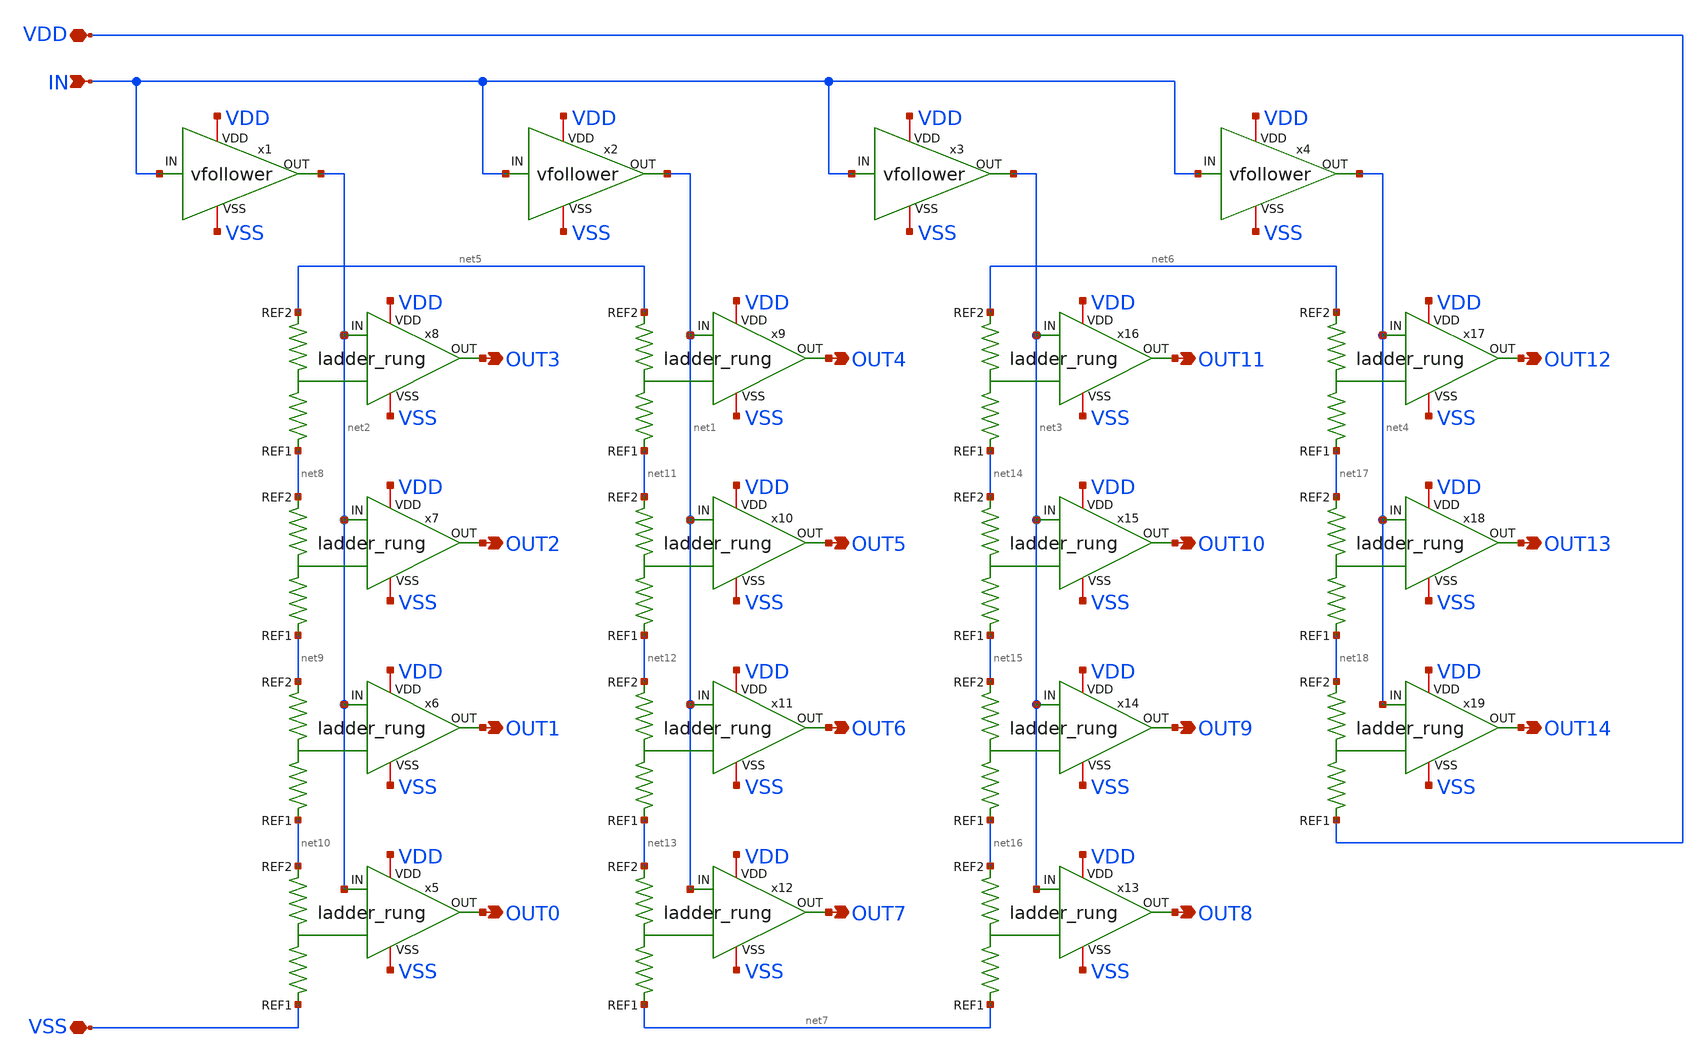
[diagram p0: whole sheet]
** sch_path: xschem/flash_adc.sch
**.subckt flash_adc VDD VSS IN OUT0 OUT1 OUT2 OUT3 OUT4 OUT5 OUT6 OUT7 OUT8 OUT9 OUT10 OUT11 OUT12
*+ OUT13 OUT14
*.iopin VDD
*.iopin VSS
*.ipin IN
*.opin OUT0
*.opin OUT1
*.opin OUT2
*.opin OUT3
*.opin OUT4
*.opin OUT5
*.opin OUT6
*.opin OUT7
*.opin OUT8
*.opin OUT9
*.opin OUT10
*.opin OUT11
*.opin OUT12
*.opin OUT13
*.opin OUT14
x1 VDD net2 IN VSS vfollower
x2 VDD net1 IN VSS vfollower
x3 VDD net3 IN VSS vfollower
x4 VDD net4 IN VSS vfollower
x5 net10 VDD net2 OUT0 VSS VSS ladder_rung
x6 net9 VDD net2 OUT1 VSS net10 ladder_rung
x7 net8 VDD net2 OUT2 VSS net9 ladder_rung
x8 net5 VDD net2 OUT3 VSS net8 ladder_rung
x9 net5 VDD net1 OUT4 VSS net11 ladder_rung
x10 net11 VDD net1 OUT5 VSS net12 ladder_rung
x11 net12 VDD net1 OUT6 VSS net13 ladder_rung
x12 net13 VDD net1 OUT7 VSS net7 ladder_rung
x13 net16 VDD net3 OUT8 VSS net7 ladder_rung
x14 net15 VDD net3 OUT9 VSS net16 ladder_rung
x15 net14 VDD net3 OUT10 VSS net15 ladder_rung
x16 net6 VDD net3 OUT11 VSS net14 ladder_rung
x17 net6 VDD net4 OUT12 VSS net17 ladder_rung
x18 net17 VDD net4 OUT13 VSS net18 ladder_rung
x19 net18 VDD net4 OUT14 VSS VDD ladder_rung
**.ends

* expanding   symbol:  vfollower.sym # of pins=4
** sym_path: xschem/vfollower.sym
** sch_path: xschem/vfollower.sch
.subckt vfollower VDD OUT IN VSS
*.iopin VDD
*.iopin VSS
*.ipin IN
*.opin OUT
x1 VDD OUT IN OUT VSS opamp
.ends


* expanding   symbol:  ladder_rung.sym # of pins=6
** sym_path: xschem/ladder_rung.sym
** sch_path: xschem/ladder_rung.sch
.subckt ladder_rung REF2 VDD IN OUT VSS REF1
*.opin OUT
*.iopin VDD
*.iopin VSS
*.ipin IN
*.iopin REF1
*.iopin REF2
XR1 REF1 net1 VSS sky130_fd_pr__res_xhigh_po_0p35 L=2.34 mult=1 m=1
x5 VDD OUT IN net1 VSS comparator
XR2 net1 REF2 VSS sky130_fd_pr__res_xhigh_po_0p35 L=2.34 mult=1 m=1
.ends


* expanding   symbol:  opamp.sym # of pins=5
** sym_path: xschem/opamp.sym
** sch_path: xschem/opamp.sch
.subckt opamp VDD OUT P N VSS
*.iopin VDD
*.iopin VSS
*.ipin P
*.ipin N
*.opin OUT
XR1 net2 VDD VSS sky130_fd_pr__res_xhigh_po_0p35 L=24.36 mult=1 m=1
XM1 net2 net2 VSS VSS sky130_fd_pr__nfet_g5v0d10v5 L=1 W=2 nf=1 ad='int((nf+1)/2) * W/nf * 0.29' as='int((nf+2)/2) * W/nf * 0.29'
+ pd='2*int((nf+1)/2) * (W/nf + 0.29)' ps='2*int((nf+2)/2) * (W/nf + 0.29)' nrd='0.29 / W' nrs='0.29 / W'
+ sa=0 sb=0 sd=0 mult=2 m=2
XM7 net1 net1 VDD VDD sky130_fd_pr__pfet_g5v0d10v5 L=1 W=4 nf=1 ad='int((nf+1)/2) * W/nf * 0.29' as='int((nf+2)/2) * W/nf * 0.29'
+ pd='2*int((nf+1)/2) * (W/nf + 0.29)' ps='2*int((nf+2)/2) * (W/nf + 0.29)' nrd='0.29 / W' nrs='0.29 / W'
+ sa=0 sb=0 sd=0 mult=2 m=2
XM8 OUT net1 VDD VDD sky130_fd_pr__pfet_g5v0d10v5 L=1 W=4 nf=1 ad='int((nf+1)/2) * W/nf * 0.29' as='int((nf+2)/2) * W/nf * 0.29'
+ pd='2*int((nf+1)/2) * (W/nf + 0.29)' ps='2*int((nf+2)/2) * (W/nf + 0.29)' nrd='0.29 / W' nrs='0.29 / W'
+ sa=0 sb=0 sd=0 mult=2 m=2
XM4 net6 net2 VSS VSS sky130_fd_pr__nfet_g5v0d10v5 L=1 W=2 nf=1 ad='int((nf+1)/2) * W/nf * 0.29' as='int((nf+2)/2) * W/nf * 0.29'
+ pd='2*int((nf+1)/2) * (W/nf + 0.29)' ps='2*int((nf+2)/2) * (W/nf + 0.29)' nrd='0.29 / W' nrs='0.29 / W'
+ sa=0 sb=0 sd=0 mult=2 m=2
XM5 net1 P net6 VSS sky130_fd_pr__nfet_g5v0d10v5 L=1 W=2 nf=1 ad='int((nf+1)/2) * W/nf * 0.29' as='int((nf+2)/2) * W/nf * 0.29'
+ pd='2*int((nf+1)/2) * (W/nf + 0.29)' ps='2*int((nf+2)/2) * (W/nf + 0.29)' nrd='0.29 / W' nrs='0.29 / W'
+ sa=0 sb=0 sd=0 mult=2 m=2
XM6 OUT N net6 VSS sky130_fd_pr__nfet_g5v0d10v5 L=1 W=2 nf=1 ad='int((nf+1)/2) * W/nf * 0.29' as='int((nf+2)/2) * W/nf * 0.29'
+ pd='2*int((nf+1)/2) * (W/nf + 0.29)' ps='2*int((nf+2)/2) * (W/nf + 0.29)' nrd='0.29 / W' nrs='0.29 / W'
+ sa=0 sb=0 sd=0 mult=2 m=2
XM2 net5 net2 VSS VSS sky130_fd_pr__nfet_g5v0d10v5 L=1 W=2 nf=1 ad='int((nf+1)/2) * W/nf * 0.29' as='int((nf+2)/2) * W/nf * 0.29'
+ pd='2*int((nf+1)/2) * (W/nf + 0.29)' ps='2*int((nf+2)/2) * (W/nf + 0.29)' nrd='0.29 / W' nrs='0.29 / W'
+ sa=0 sb=0 sd=0 mult=2 m=2
XM9 net4 net5 VDD VDD sky130_fd_pr__pfet_g5v0d10v5 L=1 W=4 nf=1 ad='int((nf+1)/2) * W/nf * 0.29' as='int((nf+2)/2) * W/nf * 0.29'
+ pd='2*int((nf+1)/2) * (W/nf + 0.29)' ps='2*int((nf+2)/2) * (W/nf + 0.29)' nrd='0.29 / W' nrs='0.29 / W'
+ sa=0 sb=0 sd=0 mult=2 m=2
XM3 VDD net5 net5 VDD sky130_fd_pr__pfet_g5v0d10v5 L=1 W=4 nf=1 ad='int((nf+1)/2) * W/nf * 0.29' as='int((nf+2)/2) * W/nf * 0.29'
+ pd='2*int((nf+1)/2) * (W/nf + 0.29)' ps='2*int((nf+2)/2) * (W/nf + 0.29)' nrd='0.29 / W' nrs='0.29 / W'
+ sa=0 sb=0 sd=0 mult=2 m=2
XM10 net3 P net4 VDD sky130_fd_pr__pfet_g5v0d10v5 L=1 W=4 nf=1 ad='int((nf+1)/2) * W/nf * 0.29' as='int((nf+2)/2) * W/nf * 0.29'
+ pd='2*int((nf+1)/2) * (W/nf + 0.29)' ps='2*int((nf+2)/2) * (W/nf + 0.29)' nrd='0.29 / W' nrs='0.29 / W'
+ sa=0 sb=0 sd=0 mult=2 m=2
XM11 OUT N net4 VDD sky130_fd_pr__pfet_g5v0d10v5 L=1 W=4 nf=1 ad='int((nf+1)/2) * W/nf * 0.29' as='int((nf+2)/2) * W/nf * 0.29'
+ pd='2*int((nf+1)/2) * (W/nf + 0.29)' ps='2*int((nf+2)/2) * (W/nf + 0.29)' nrd='0.29 / W' nrs='0.29 / W'
+ sa=0 sb=0 sd=0 mult=2 m=2
XM12 net3 net3 VSS VSS sky130_fd_pr__nfet_g5v0d10v5 L=1 W=2 nf=1 ad='int((nf+1)/2) * W/nf * 0.29' as='int((nf+2)/2) * W/nf * 0.29'
+ pd='2*int((nf+1)/2) * (W/nf + 0.29)' ps='2*int((nf+2)/2) * (W/nf + 0.29)' nrd='0.29 / W' nrs='0.29 / W'
+ sa=0 sb=0 sd=0 mult=2 m=2
XM13 OUT net3 VSS VSS sky130_fd_pr__nfet_g5v0d10v5 L=1 W=2 nf=1 ad='int((nf+1)/2) * W/nf * 0.29' as='int((nf+2)/2) * W/nf * 0.29'
+ pd='2*int((nf+1)/2) * (W/nf + 0.29)' ps='2*int((nf+2)/2) * (W/nf + 0.29)' nrd='0.29 / W' nrs='0.29 / W'
+ sa=0 sb=0 sd=0 mult=2 m=2
.ends


* expanding   symbol:  comparator.sym # of pins=5
** sym_path: xschem/comparator.sym
** sch_path: xschem/comparator.sch
.subckt comparator VDD OUT P N VSS
*.iopin VDD
*.iopin VSS
*.ipin P
*.ipin N
*.opin OUT
x1 VDD net1 P N VSS opamp
x2 VDD OUT net1 VSS buffer
.ends


* expanding   symbol:  buffer.sym # of pins=4
** sym_path: xschem/buffer.sym
** sch_path: xschem/buffer.sch
.subckt buffer VDD OUT IN VSS
*.iopin VDD
*.iopin VSS
*.ipin IN
*.opin OUT
XM1 net1 IN VSS VSS sky130_fd_pr__nfet_g5v0d10v5 L=0.5 W=0.5 nf=1 ad='int((nf+1)/2) * W/nf * 0.29' as='int((nf+2)/2) * W/nf * 0.29'
+ pd='2*int((nf+1)/2) * (W/nf + 0.29)' ps='2*int((nf+2)/2) * (W/nf + 0.29)' nrd='0.29 / W' nrs='0.29 / W'
+ sa=0 sb=0 sd=0 mult=1 m=1
XM2 net1 IN VDD VDD sky130_fd_pr__pfet_g5v0d10v5 L=0.5 W=1 nf=1 ad='int((nf+1)/2) * W/nf * 0.29' as='int((nf+2)/2) * W/nf * 0.29'
+ pd='2*int((nf+1)/2) * (W/nf + 0.29)' ps='2*int((nf+2)/2) * (W/nf + 0.29)' nrd='0.29 / W' nrs='0.29 / W'
+ sa=0 sb=0 sd=0 mult=1 m=1
XM3 OUT net1 VSS VSS sky130_fd_pr__nfet_g5v0d10v5 L=0.5 W=0.5 nf=1 ad='int((nf+1)/2) * W/nf * 0.29' as='int((nf+2)/2) * W/nf * 0.29'
+ pd='2*int((nf+1)/2) * (W/nf + 0.29)' ps='2*int((nf+2)/2) * (W/nf + 0.29)' nrd='0.29 / W' nrs='0.29 / W'
+ sa=0 sb=0 sd=0 mult=1 m=1
XM4 OUT net1 VDD VDD sky130_fd_pr__pfet_g5v0d10v5 L=0.5 W=1 nf=1 ad='int((nf+1)/2) * W/nf * 0.29' as='int((nf+2)/2) * W/nf * 0.29'
+ pd='2*int((nf+1)/2) * (W/nf + 0.29)' ps='2*int((nf+2)/2) * (W/nf + 0.29)' nrd='0.29 / W' nrs='0.29 / W'
+ sa=0 sb=0 sd=0 mult=1 m=1
.ends

.end
